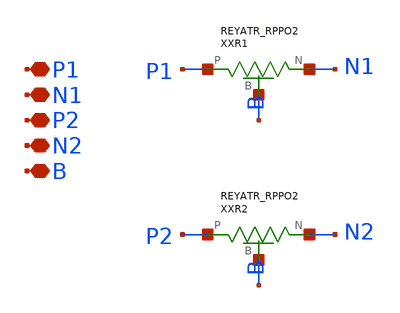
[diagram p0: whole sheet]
** sch_path: design/LELO_TEMP_SKY130A/REYATR_RESABUTR.sch
**.subckt REYATR_RESABUTR P1 N1 P2 N2 B
*.iopin P1
*.iopin N1
*.iopin P2
*.iopin N2
*.iopin B
XXR1 N1 P1 B REYATR_RPPO2
XXR2 N2 P2 B REYATR_RPPO2
**.ends
.end
